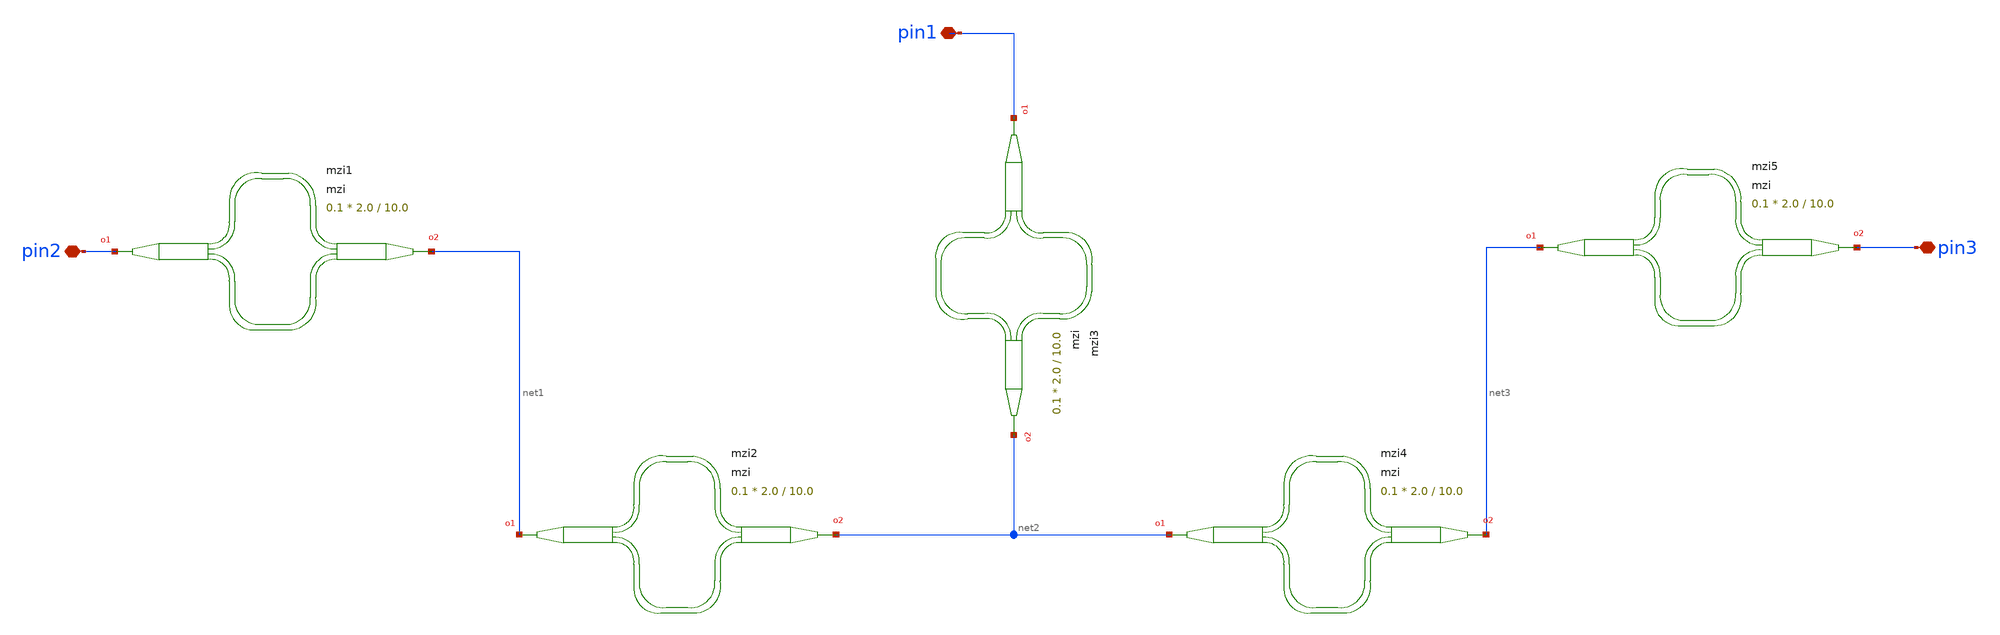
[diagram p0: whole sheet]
** sch_path: cells/xschem/tests/test_mzi.sch
* SPDX-FileCopyrightText: 2023 Mabrains Company
* Licensed under the GNU GENERAL PUBLIC License, Version 3.0 (the "License");
* you may not use this file except in compliance with the License.
* GNU GENERAL PUBLIC LICENSE
* Version 3, 29 June 2007
* This program is free software: you can redistribute it and/or modify
* it under the terms of the GNU General Public License as published
* by the Free Software Foundation, either 3 of the License, or
* (at your option) any later version.
* This program is distributed in the hope that it will be useful,
* but WITHOUT ANY WARRANTY; without even the implied warranty of
* MERCHANTABILITY or FITNESS FOR A PARTICULAR PURPOSE.  See the
* GNU General Public License for more details.
* You should have received a copy of the GNU General Public License
* along with this program.  If not, see <https://www.gnu.org/licenses/>.
* SPDX-License-Identifier: GPL-3.0
**.subckt test_mzi pin2 pin1 pin3
*.iopin pin2
*.iopin pin1
*.iopin pin3
Pmzi1 pin2 net1 mzi delta_length=10.0 length_y=2.0 length_x=0.1
Pmzi2 net1 net2 mzi delta_length=10.0 length_y=2.0 length_x=0.1
Pmzi3 pin1 net2 mzi delta_length=10.0 length_y=2.0 length_x=0.1
Pmzi4 net2 net3 mzi delta_length=10.0 length_y=2.0 length_x=0.1
Pmzi5 net3 pin3 mzi delta_length=10.0 length_y=2.0 length_x=0.1
**.ends
.end
